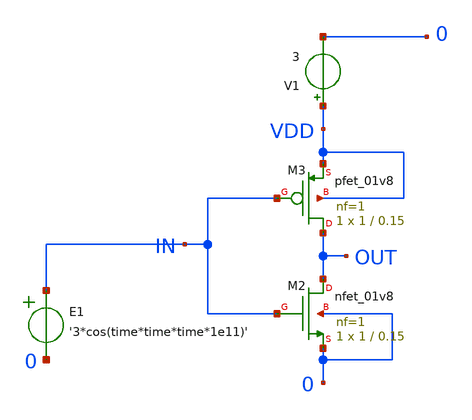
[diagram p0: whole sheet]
** sch_path: Tb_inverter.sch
**.subckt Tb_inverter
XM3 OUT IN VDD VDD sky130_fd_pr__pfet_01v8 L=0.15 W=1 nf=1 ad='int((nf+1)/2) * W/nf * 0.29' as='int((nf+2)/2) * W/nf * 0.29'
+ pd='2*int((nf+1)/2) * (W/nf + 0.29)' ps='2*int((nf+2)/2) * (W/nf + 0.29)' nrd='0.29 / W' nrs='0.29 / W'
+ sa=0 sb=0 sd=0 mult=1 m=1
XM2 OUT IN 0 0 sky130_fd_pr__nfet_01v8 L=0.15 W=1 nf=1 ad='int((nf+1)/2) * W/nf * 0.29' as='int((nf+2)/2) * W/nf * 0.29'
+ pd='2*int((nf+1)/2) * (W/nf + 0.29)' ps='2*int((nf+2)/2) * (W/nf + 0.29)' nrd='0.29 / W' nrs='0.29 / W'
+ sa=0 sb=0 sd=0 mult=1 m=1
E1 IN 0 VOL=' '3*cos(time*time*time*1e11)' '
V1 VDD 0 3
**** begin user architecture code


.tran 10n 2000u uic
.save all


**** end user architecture code
**.ends
.end
